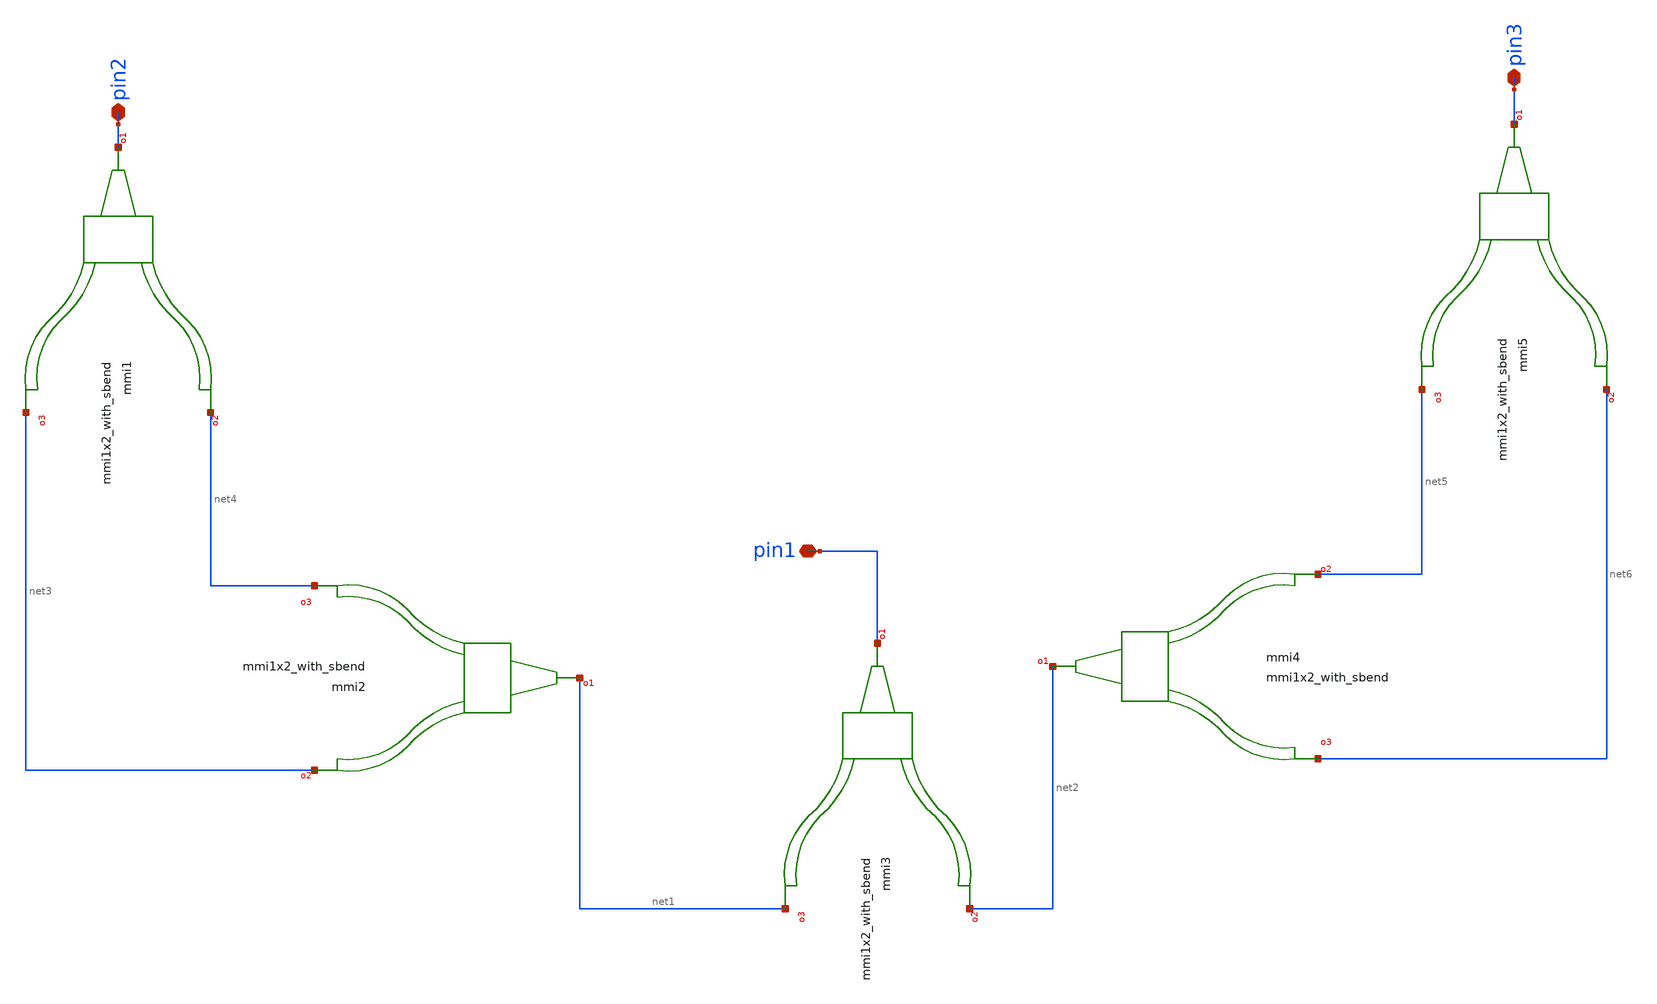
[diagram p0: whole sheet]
** sch_path: xschem/tests/test_sch/test_mmi1x2_with_sbend.sch
* Copyright (c) 2024, Mabrains LLC
* Licensed under the GNU Lesser General Public License, Version 3.0 (the "License");
* you may not use this file except in compliance with the License.
* GNU Lesser General Public License
* Version 3, 29 June 2007
* This program is free software: you can redistribute it and/or modify
* it under the terms of the GNU Lesser General Public License as published
* by the Free Software Foundation, either version 3 of the License, or
* (at your option) any later version.
* This program is distributed in the hope that it will be useful,
* but WITHOUT ANY WARRANTY; without even the implied warranty of
* MERCHANTABILITY or FITNESS FOR A PARTICULAR PURPOSE.  See the
* GNU Lesser General Public License for more details.
* You should have received a copy of the GNU Lesser General Public License
* along with this program.  If not, see <https://www.gnu.org/licenses/>.
* SPDX-License-Identifier: LGPL-3.0
**.subckt test_mmi1x2_with_sbend pin1 pin3 pin2
*.iopin pin1
*.iopin pin3
*.iopin pin2
Pmmi1 pin2 net4 net3 mmi1x2_with_sbend
Pmmi2 net1 net3 net4 mmi1x2_with_sbend
Pmmi3 pin1 net2 net1 mmi1x2_with_sbend
Pmmi4 net2 net5 net6 mmi1x2_with_sbend
Pmmi5 pin3 net6 net5 mmi1x2_with_sbend
**.ends
.end
